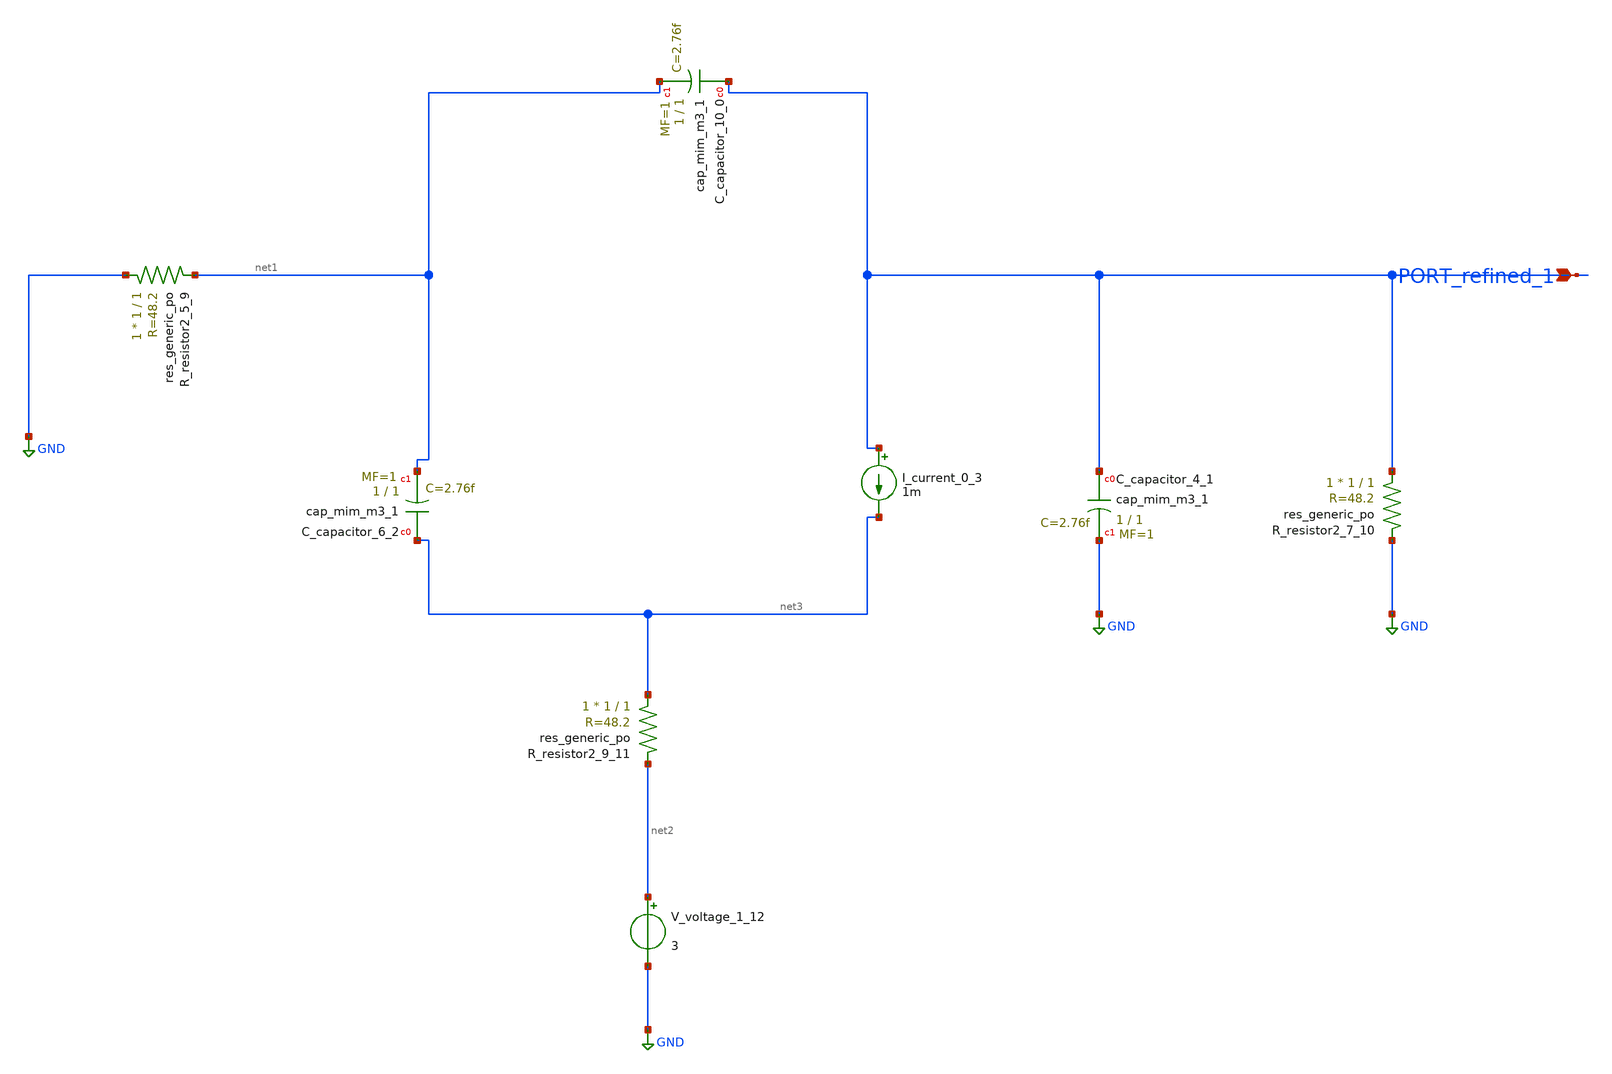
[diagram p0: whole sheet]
** sch_path: schematics/AMSNet/405.sch
**.subckt 405 PORT_refined_1
*.ipin PORT_refined_1
XC_capacitor_10_0 PORT_refined_1 net1 sky130_fd_pr__cap_mim_m3_1 W=1 L=1 MF=1 m=1
XC_capacitor_4_1 PORT_refined_1 GND sky130_fd_pr__cap_mim_m3_1 W=1 L=1 MF=1 m=1
XC_capacitor_6_2 net3 net1 sky130_fd_pr__cap_mim_m3_1 W=1 L=1 MF=1 m=1
I_current_0_3 PORT_refined_1 net3 1m
XR_resistor2_5_9 GND net1 sky130_fd_pr__res_generic_po W=1 L=1 m=1
XR_resistor2_7_10 PORT_refined_1 GND sky130_fd_pr__res_generic_po W=1 L=1 m=1
XR_resistor2_9_11 net3 net2 sky130_fd_pr__res_generic_po W=1 L=1 m=1
V_voltage_1_12 net2 GND 3
**.ends
.GLOBAL GND
.end
